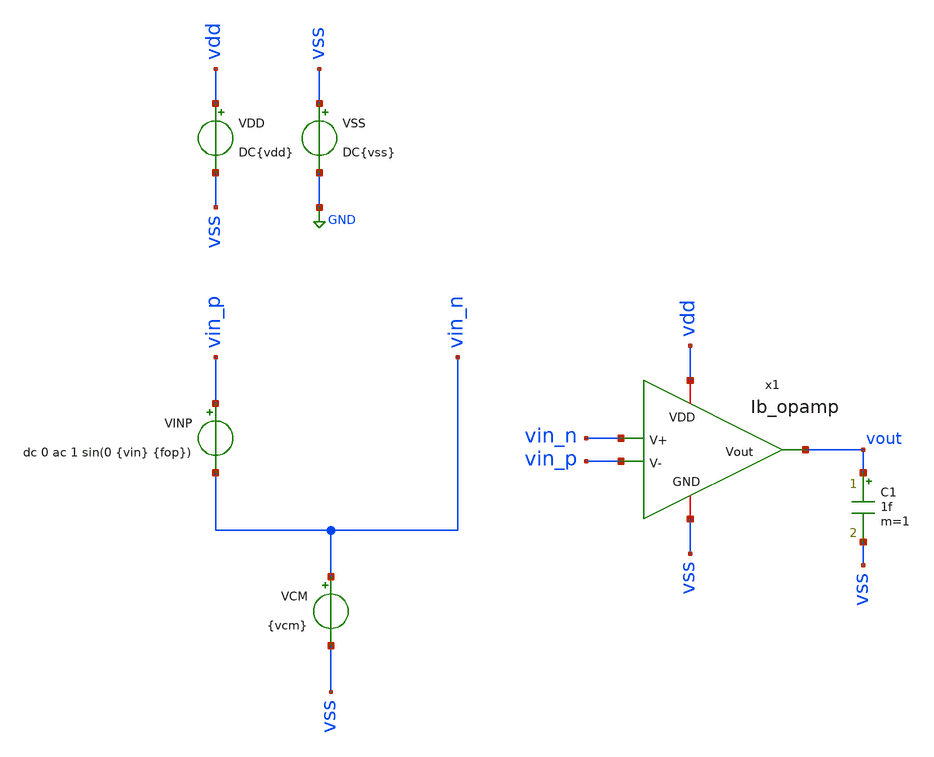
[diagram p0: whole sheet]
** sch_path: SSDOR_1.2V_v4/components/Ibias_uA/ibias_opamp/tb_opamp.sch
**.subckt tb_opamp
VDD vdd vss DC{vdd}
VSS vss GND DC{vss}
VCM vin_n vss {vcm}
C1 vout vss 1f m=1
VINP vin_p vin_n dc 0 ac 1 sin(0 {vin} {fop})
x1 vdd vout vin_p vin_n vss Ib_opamp
**** begin user architecture code



* Parameters
.param vdd = 1
.param vss = 0.0
.param vin = 0.5
.param vcm = 500m
.param fop = 13.56Meg

* Models
.lib cornerMOSlv.lib mos_tt

* Data to save
.save all

* Simulation
.control

 set color0 = white

 *tran 500p 0.5u
 *let vac = vin_p-vin_n
 *plot v(vac) v(vout)

 ac dec 100 1 50G
 meas ac GBW when vdb(vout)=0
 meas ac DCG find vdb(vout) at=0
 meas ac PM find vp(vout) when vdb(vout)=0
 print PM*180/PI
 plot vdb(vout) {vp(vout)*180/PI}

 reset
 op
 write tb_opamp.raw

.endc



**** end user architecture code
**.ends
.GLOBAL GND
.end
